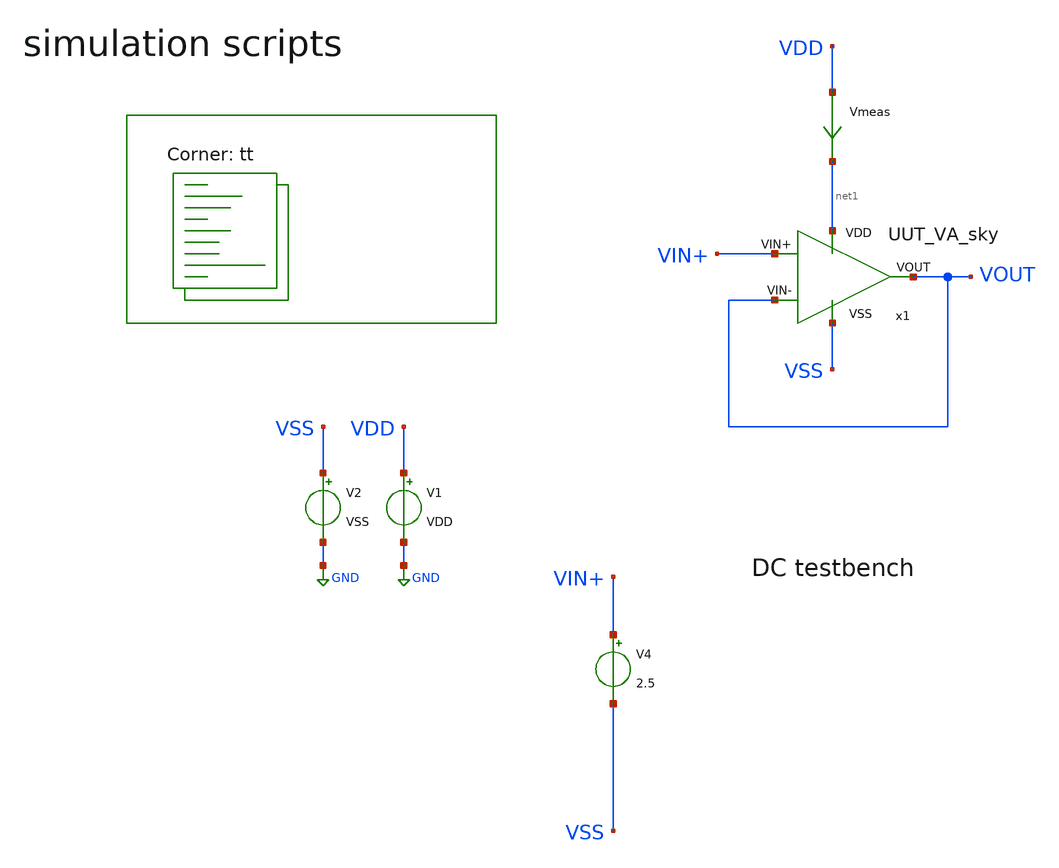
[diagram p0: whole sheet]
** sch_path: Learning/single_ended_amplifiers/Design_and_Analysis_of_Two-Stage_CMOS_Operational_Amplifier_for_Fluorescence_Signal_Processing_sky130_5V/amplifier_design/OTA_DC_TB.sch
**.subckt OTA_DC_TB
V1 VDD GND VDD
V2 VSS GND VSS
V4 VIN+ VSS 2.5
Vmeas VDD net1 0
.save i(vmeas)
x1 net1 VSS VOUT VIN+ VOUT UUT_VA_sky
**** begin user architecture code
.lib $::SKYWATER_MODELS/sky130.lib.spice tt

.Temp 27
.param VDD = 1.8
.param VSS = 0

.control
save all
dc V4 0 5 0.01
wrdata VIN_sweep_DC.csv v(VOUT) i(Vmeas)
plot v(VOUT) v(VIN+)
plot i(Vmeas)

.endc

**** end user architecture code
**.ends

* expanding   symbol:  Sky130A/UUT_sky/UUT_VA_sky.sym # of pins=5
** sym_path: my_ip/LIB/Sky130A/UUT_sky/UUT_VA_sky.sym
** sch_path: my_ip/LIB/Sky130A/UUT_sky/UUT_VA_sky.sch
.subckt UUT_VA_sky VDD VSS VIN- VIN+ VOUT
*.iopin VDD
*.iopin VSS
*.iopin VIN-
*.iopin VIN+
*.iopin VOUT
x1 VDD VSS VIN+ VIN- VOUT A001
.ends

.GLOBAL GND
.end
